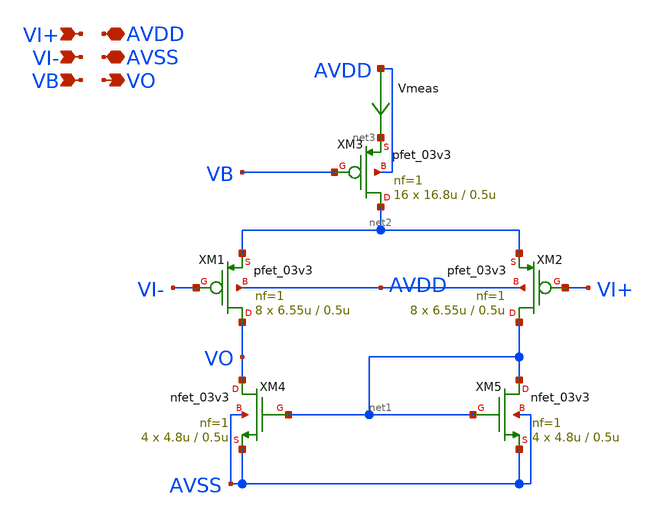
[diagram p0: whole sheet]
** sch_path: designs/libs/core_analog/ota_5t/ota_5t.sch
**.subckt ota_5t VI+ VI- VB AVDD AVSS VO
*.ipin VI+
*.ipin VI-
*.ipin VB
*.iopin AVDD
*.iopin AVSS
*.opin VO
XM1 VO VI- net2 AVDD pfet_03v3 L=0.5u W=6.55u nf=1 ad='int((nf+1)/2) * W/nf * 0.18u' as='int((nf+2)/2) * W/nf * 0.18u'
+ pd='2*int((nf+1)/2) * (W/nf + 0.18u)' ps='2*int((nf+2)/2) * (W/nf + 0.18u)' nrd='0.18u / W' nrs='0.18u / W'
+ sa=0 sb=0 sd=0 m=8
XM4 VO net1 AVSS AVSS nfet_03v3 L=0.5u W=4.8u nf=1 ad='int((nf+1)/2) * W/nf * 0.18u' as='int((nf+2)/2) * W/nf * 0.18u'
+ pd='2*int((nf+1)/2) * (W/nf + 0.18u)' ps='2*int((nf+2)/2) * (W/nf + 0.18u)' nrd='0.18u / W' nrs='0.18u / W'
+ sa=0 sb=0 sd=0 m=4
XM3 net2 VB net3 AVDD pfet_03v3 L=0.5u W=16.8u nf=1 ad='int((nf+1)/2) * W/nf * 0.18u' as='int((nf+2)/2) * W/nf * 0.18u'
+ pd='2*int((nf+1)/2) * (W/nf + 0.18u)' ps='2*int((nf+2)/2) * (W/nf + 0.18u)' nrd='0.18u / W' nrs='0.18u / W'
+ sa=0 sb=0 sd=0 m=16
XM2 net1 VI+ net2 AVDD pfet_03v3 L=0.5u W=6.55u nf=1 ad='int((nf+1)/2) * W/nf * 0.18u' as='int((nf+2)/2) * W/nf * 0.18u'
+ pd='2*int((nf+1)/2) * (W/nf + 0.18u)' ps='2*int((nf+2)/2) * (W/nf + 0.18u)' nrd='0.18u / W' nrs='0.18u / W'
+ sa=0 sb=0 sd=0 m=8
XM5 net1 net1 AVSS AVSS nfet_03v3 L=0.5u W=4.8u nf=1 ad='int((nf+1)/2) * W/nf * 0.18u' as='int((nf+2)/2) * W/nf * 0.18u'
+ pd='2*int((nf+1)/2) * (W/nf + 0.18u)' ps='2*int((nf+2)/2) * (W/nf + 0.18u)' nrd='0.18u / W' nrs='0.18u / W'
+ sa=0 sb=0 sd=0 m=4
Vmeas AVDD net3 0
.save i(vmeas)
**.ends
.end
